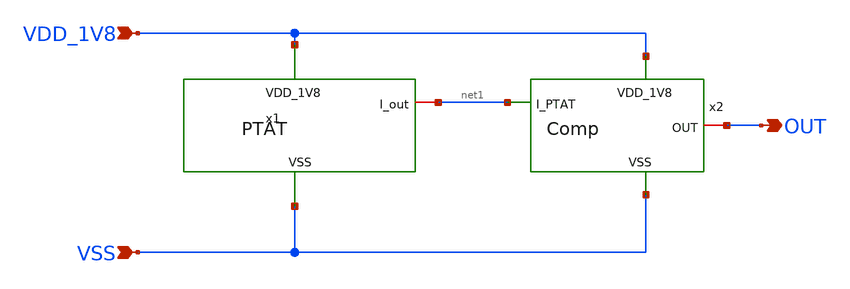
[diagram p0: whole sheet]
** sch_path: design/JNW_GR04_SKY130A/PTAT_TO_COMP.sch
**.subckt PTAT_TO_COMP VDD_1V8 VSS OUT
*.ipin VDD_1V8
*.ipin VSS
*.opin OUT
x1 VDD_1V8 net1 VSS PTAT
x2 VDD_1V8 OUT net1 VSS Comp
**.ends
.end
